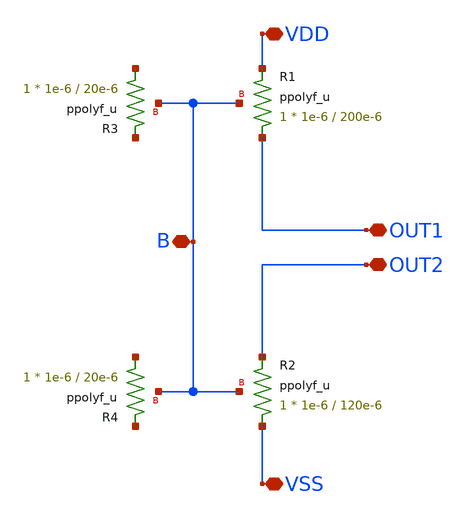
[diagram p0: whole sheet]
** sch_path: LDO/xschem/resistor/resistor.sch
**.subckt resistor OUT1 VSS VDD B OUT2
*.iopin OUT1
*.iopin VSS
*.iopin VDD
*.iopin B
*.iopin OUT2
XR1 OUT1 VDD B ppolyf_u r_width=1e-6 r_length=200e-6 m=1
XR2 VSS OUT2 B ppolyf_u r_width=1e-6 r_length=120e-6 m=1
XR3 net1 net2 B ppolyf_u r_width=1e-6 r_length=20e-6 m=1
XR4 net3 net4 B ppolyf_u r_width=1e-6 r_length=20e-6 m=1
**.ends
.end
